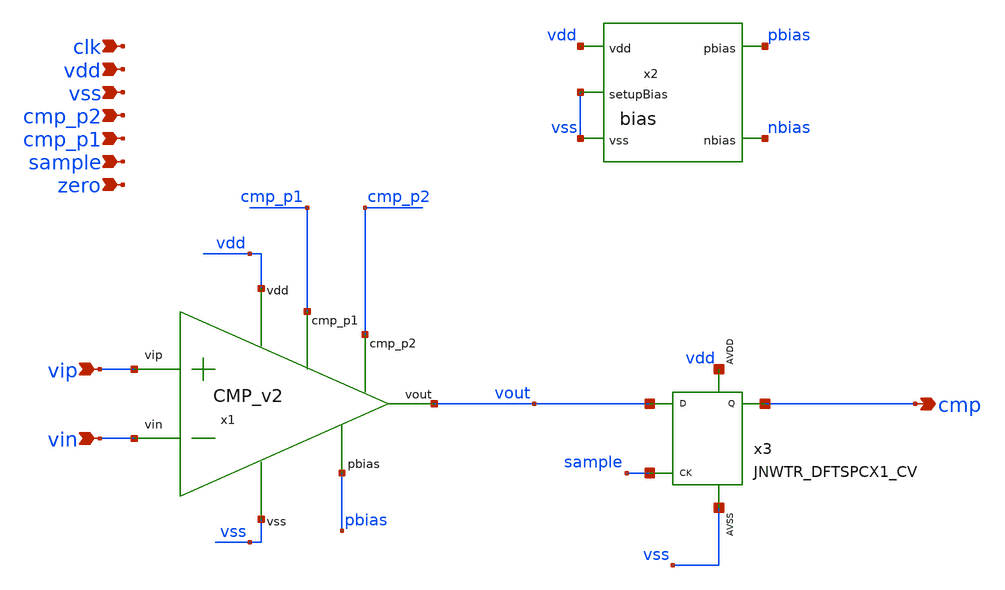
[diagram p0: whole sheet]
** sch_path: design/JNW_AVV_SKY130A/TB_CMP.sch
**.subckt TB_CMP vdd vss vip vin cmp cmp_p1 cmp_p2 clk sample zero
*.ipin vdd
*.ipin vss
*.ipin vip
*.ipin vin
*.opin cmp
*.ipin cmp_p1
*.ipin cmp_p2
*.ipin clk
*.ipin sample
*.ipin zero
x2 pbias vdd nbias vss vss bias
x1 vdd pbias vout vin vip vss cmp_p1 cmp_p2 CMP_v2
x3 vout sample cmp vdd vss JNWTR_DFTSPCX1_CV xoffset=0 yoffset=0 angle=0
**.ends
.end
